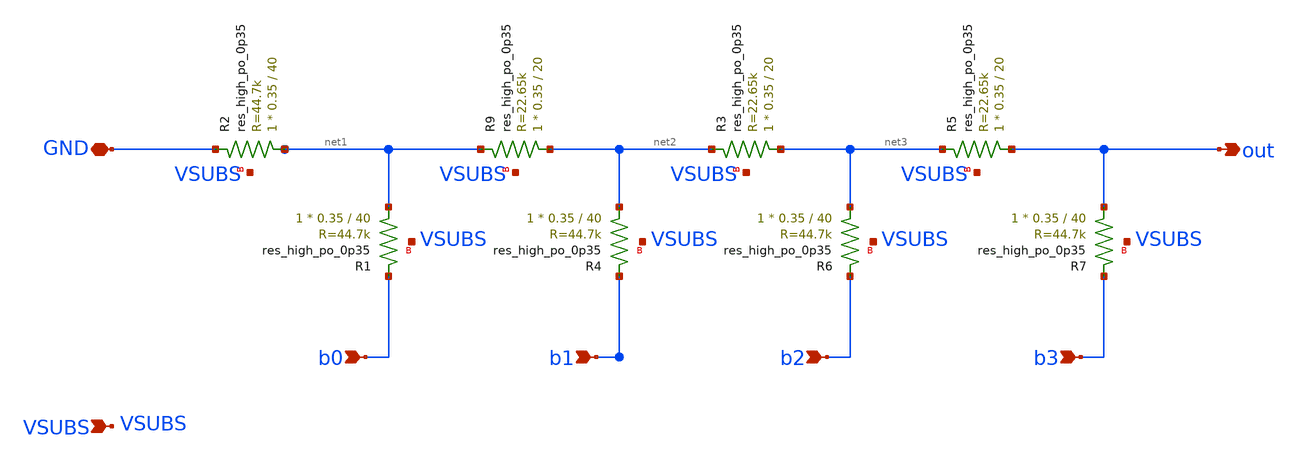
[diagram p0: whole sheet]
** sch_path: xschem/r2r_4b.sch
**.subckt r2r_4b GND out b0 b2 b1 b3 VSUBS
*.iopin GND
*.opin out
*.ipin b0
*.ipin b2
*.ipin b1
*.ipin b3
*.ipin VSUBS
XR2 net1 GND VSUBS sky130_fd_pr__res_high_po_0p35 L=40 mult=1 m=1
XR9 net2 net1 VSUBS sky130_fd_pr__res_high_po_0p35 L=20 mult=1 m=1
XR1 net1 b0 VSUBS sky130_fd_pr__res_high_po_0p35 L=40 mult=1 m=1
XR3 net3 net2 VSUBS sky130_fd_pr__res_high_po_0p35 L=20 mult=1 m=1
XR4 net2 b1 VSUBS sky130_fd_pr__res_high_po_0p35 L=40 mult=1 m=1
XR5 out net3 VSUBS sky130_fd_pr__res_high_po_0p35 L=20 mult=1 m=1
XR6 net3 b2 VSUBS sky130_fd_pr__res_high_po_0p35 L=40 mult=1 m=1
XR7 out b3 VSUBS sky130_fd_pr__res_high_po_0p35 L=40 mult=1 m=1
**.ends
.end
